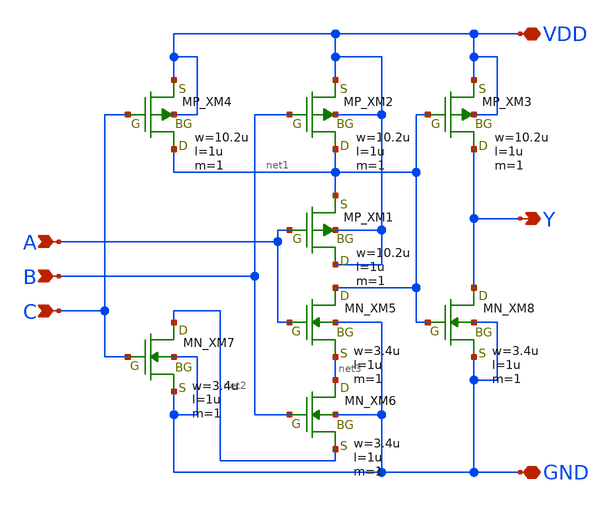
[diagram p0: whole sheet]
** sch_path: openIP62_rev1.0/IP62/Technology/tech/symbols/Xschem/IP62_5_stdcell/AND3_X1.sch
**.subckt AND3_X1 Y A B VDD GND C
*.opin Y
*.ipin A
*.ipin B
*.iopin VDD
*.iopin GND
*.ipin C
XM4 net1 C VDD VDD PMOS w=10.2u l=1u as=0 ad=0 ps=0 pd=0 nrd=0 nrs=0 m=1
XM2 net1 B VDD VDD PMOS w=10.2u l=1u as=0 ad=0 ps=0 pd=0 nrd=0 nrs=0 m=1
XM3 Y net1 VDD VDD PMOS w=10.2u l=1u as=0 ad=0 ps=0 pd=0 nrd=0 nrs=0 m=1
XM1 VDD A net1 VDD PMOS w=10.2u l=1u as=0 ad=0 ps=0 pd=0 nrd=0 nrs=0 m=1
XM8 Y net1 GND GND NMOS w=3.4u l=1u as=0 ad=0 ps=0 pd=0 nrd=0 nrs=0 m=1
XM5 net1 A net3 GND NMOS w=3.4u l=1u as=0 ad=0 ps=0 pd=0 nrd=0 nrs=0 m=1
XM6 net3 B net2 GND NMOS w=3.4u l=1u as=0 ad=0 ps=0 pd=0 nrd=0 nrs=0 m=1
XM7 net2 C GND GND NMOS w=3.4u l=1u as=0 ad=0 ps=0 pd=0 nrd=0 nrs=0 m=1
**.ends
.end
